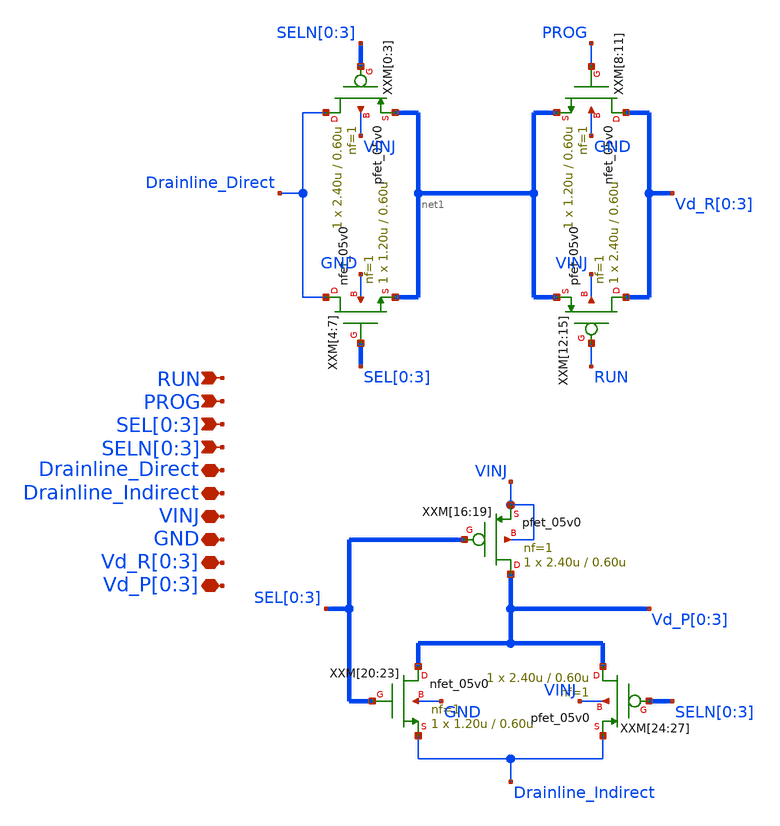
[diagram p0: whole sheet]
** sch_path: drain_switch/schematic/SWC_Drain.sch
**.subckt SWC_Drain RUN PROG SEL[0],SEL[1],SEL[2],SEL[3] SELN[0],SELN[1],SELN[2],SELN[3]
*+ Drainline_Direct Drainline_Indirect VINJ GND Vd_R[0],Vd_R[1],Vd_R[2],Vd_R[3] Vd_P[0],Vd_P[1],Vd_P[2],Vd_P[3]
*.ipin RUN
*.ipin PROG
*.ipin SEL[0],SEL[1],SEL[2],SEL[3]
*.ipin SELN[0],SELN[1],SELN[2],SELN[3]
*.iopin Drainline_Direct
*.iopin Drainline_Indirect
*.iopin VINJ
*.iopin GND
*.iopin Vd_R[0],Vd_R[1],Vd_R[2],Vd_R[3]
*.iopin Vd_P[0],Vd_P[1],Vd_P[2],Vd_P[3]
XXM[4] Drainline_Direct SEL[0] net1[3] GND nfet_05v0 L=0.60u W=1.20u nf=1 ad='int((nf+1)/2) * W/nf * 0.18u'
+ as='int((nf+2)/2) * W/nf * 0.18u' pd='2*int((nf+1)/2) * (W/nf + 0.18u)' ps='2*int((nf+2)/2) * (W/nf + 0.18u)'
+ nrd='0.18u / W' nrs='0.18u / W' sa=0 sb=0 sd=0 m=1
XXM[5] Drainline_Direct SEL[1] net1[2] GND nfet_05v0 L=0.60u W=1.20u nf=1 ad='int((nf+1)/2) * W/nf * 0.18u'
+ as='int((nf+2)/2) * W/nf * 0.18u' pd='2*int((nf+1)/2) * (W/nf + 0.18u)' ps='2*int((nf+2)/2) * (W/nf + 0.18u)'
+ nrd='0.18u / W' nrs='0.18u / W' sa=0 sb=0 sd=0 m=1
XXM[6] Drainline_Direct SEL[2] net1[1] GND nfet_05v0 L=0.60u W=1.20u nf=1 ad='int((nf+1)/2) * W/nf * 0.18u'
+ as='int((nf+2)/2) * W/nf * 0.18u' pd='2*int((nf+1)/2) * (W/nf + 0.18u)' ps='2*int((nf+2)/2) * (W/nf + 0.18u)'
+ nrd='0.18u / W' nrs='0.18u / W' sa=0 sb=0 sd=0 m=1
XXM[7] Drainline_Direct SEL[3] net1[0] GND nfet_05v0 L=0.60u W=1.20u nf=1 ad='int((nf+1)/2) * W/nf * 0.18u'
+ as='int((nf+2)/2) * W/nf * 0.18u' pd='2*int((nf+1)/2) * (W/nf + 0.18u)' ps='2*int((nf+2)/2) * (W/nf + 0.18u)'
+ nrd='0.18u / W' nrs='0.18u / W' sa=0 sb=0 sd=0 m=1
XXM[0] Drainline_Direct SELN[0] net1[3] VINJ pfet_05v0 L=0.60u W=2.40u nf=1 ad='int((nf+1)/2) * W/nf * 0.18u'
+ as='int((nf+2)/2) * W/nf * 0.18u' pd='2*int((nf+1)/2) * (W/nf + 0.18u)' ps='2*int((nf+2)/2) * (W/nf + 0.18u)'
+ nrd='0.18u / W' nrs='0.18u / W' sa=0 sb=0 sd=0 m=1
XXM[1] Drainline_Direct SELN[1] net1[2] VINJ pfet_05v0 L=0.60u W=2.40u nf=1 ad='int((nf+1)/2) * W/nf * 0.18u'
+ as='int((nf+2)/2) * W/nf * 0.18u' pd='2*int((nf+1)/2) * (W/nf + 0.18u)' ps='2*int((nf+2)/2) * (W/nf + 0.18u)'
+ nrd='0.18u / W' nrs='0.18u / W' sa=0 sb=0 sd=0 m=1
XXM[2] Drainline_Direct SELN[2] net1[1] VINJ pfet_05v0 L=0.60u W=2.40u nf=1 ad='int((nf+1)/2) * W/nf * 0.18u'
+ as='int((nf+2)/2) * W/nf * 0.18u' pd='2*int((nf+1)/2) * (W/nf + 0.18u)' ps='2*int((nf+2)/2) * (W/nf + 0.18u)'
+ nrd='0.18u / W' nrs='0.18u / W' sa=0 sb=0 sd=0 m=1
XXM[3] Drainline_Direct SELN[3] net1[0] VINJ pfet_05v0 L=0.60u W=2.40u nf=1 ad='int((nf+1)/2) * W/nf * 0.18u'
+ as='int((nf+2)/2) * W/nf * 0.18u' pd='2*int((nf+1)/2) * (W/nf + 0.18u)' ps='2*int((nf+2)/2) * (W/nf + 0.18u)'
+ nrd='0.18u / W' nrs='0.18u / W' sa=0 sb=0 sd=0 m=1
XXM[8] Vd_R[0] PROG net1[3] GND nfet_05v0 L=0.60u W=1.20u nf=1 ad='int((nf+1)/2) * W/nf * 0.18u' as='int((nf+2)/2) * W/nf * 0.18u'
+ pd='2*int((nf+1)/2) * (W/nf + 0.18u)' ps='2*int((nf+2)/2) * (W/nf + 0.18u)' nrd='0.18u / W' nrs='0.18u / W'
+ sa=0 sb=0 sd=0 m=1
XXM[9] Vd_R[1] PROG net1[2] GND nfet_05v0 L=0.60u W=1.20u nf=1 ad='int((nf+1)/2) * W/nf * 0.18u' as='int((nf+2)/2) * W/nf * 0.18u'
+ pd='2*int((nf+1)/2) * (W/nf + 0.18u)' ps='2*int((nf+2)/2) * (W/nf + 0.18u)' nrd='0.18u / W' nrs='0.18u / W'
+ sa=0 sb=0 sd=0 m=1
XXM[10] Vd_R[2] PROG net1[1] GND nfet_05v0 L=0.60u W=1.20u nf=1 ad='int((nf+1)/2) * W/nf * 0.18u' as='int((nf+2)/2) * W/nf * 0.18u'
+ pd='2*int((nf+1)/2) * (W/nf + 0.18u)' ps='2*int((nf+2)/2) * (W/nf + 0.18u)' nrd='0.18u / W' nrs='0.18u / W'
+ sa=0 sb=0 sd=0 m=1
XXM[11] Vd_R[3] PROG net1[0] GND nfet_05v0 L=0.60u W=1.20u nf=1 ad='int((nf+1)/2) * W/nf * 0.18u' as='int((nf+2)/2) * W/nf * 0.18u'
+ pd='2*int((nf+1)/2) * (W/nf + 0.18u)' ps='2*int((nf+2)/2) * (W/nf + 0.18u)' nrd='0.18u / W' nrs='0.18u / W'
+ sa=0 sb=0 sd=0 m=1
XXM[12] Vd_R[0] RUN net1[3] VINJ pfet_05v0 L=0.60u W=2.40u nf=1 ad='int((nf+1)/2) * W/nf * 0.18u' as='int((nf+2)/2) * W/nf * 0.18u'
+ pd='2*int((nf+1)/2) * (W/nf + 0.18u)' ps='2*int((nf+2)/2) * (W/nf + 0.18u)' nrd='0.18u / W' nrs='0.18u / W'
+ sa=0 sb=0 sd=0 m=1
XXM[13] Vd_R[1] RUN net1[2] VINJ pfet_05v0 L=0.60u W=2.40u nf=1 ad='int((nf+1)/2) * W/nf * 0.18u' as='int((nf+2)/2) * W/nf * 0.18u'
+ pd='2*int((nf+1)/2) * (W/nf + 0.18u)' ps='2*int((nf+2)/2) * (W/nf + 0.18u)' nrd='0.18u / W' nrs='0.18u / W'
+ sa=0 sb=0 sd=0 m=1
XXM[14] Vd_R[2] RUN net1[1] VINJ pfet_05v0 L=0.60u W=2.40u nf=1 ad='int((nf+1)/2) * W/nf * 0.18u' as='int((nf+2)/2) * W/nf * 0.18u'
+ pd='2*int((nf+1)/2) * (W/nf + 0.18u)' ps='2*int((nf+2)/2) * (W/nf + 0.18u)' nrd='0.18u / W' nrs='0.18u / W'
+ sa=0 sb=0 sd=0 m=1
XXM[15] Vd_R[3] RUN net1[0] VINJ pfet_05v0 L=0.60u W=2.40u nf=1 ad='int((nf+1)/2) * W/nf * 0.18u' as='int((nf+2)/2) * W/nf * 0.18u'
+ pd='2*int((nf+1)/2) * (W/nf + 0.18u)' ps='2*int((nf+2)/2) * (W/nf + 0.18u)' nrd='0.18u / W' nrs='0.18u / W'
+ sa=0 sb=0 sd=0 m=1
XXM[20] Vd_P[0] SEL[0] Drainline_Indirect GND nfet_05v0 L=0.60u W=1.20u nf=1 ad='int((nf+1)/2) * W/nf * 0.18u'
+ as='int((nf+2)/2) * W/nf * 0.18u' pd='2*int((nf+1)/2) * (W/nf + 0.18u)' ps='2*int((nf+2)/2) * (W/nf + 0.18u)'
+ nrd='0.18u / W' nrs='0.18u / W' sa=0 sb=0 sd=0 m=1
XXM[21] Vd_P[1] SEL[1] Drainline_Indirect GND nfet_05v0 L=0.60u W=1.20u nf=1 ad='int((nf+1)/2) * W/nf * 0.18u'
+ as='int((nf+2)/2) * W/nf * 0.18u' pd='2*int((nf+1)/2) * (W/nf + 0.18u)' ps='2*int((nf+2)/2) * (W/nf + 0.18u)'
+ nrd='0.18u / W' nrs='0.18u / W' sa=0 sb=0 sd=0 m=1
XXM[22] Vd_P[2] SEL[2] Drainline_Indirect GND nfet_05v0 L=0.60u W=1.20u nf=1 ad='int((nf+1)/2) * W/nf * 0.18u'
+ as='int((nf+2)/2) * W/nf * 0.18u' pd='2*int((nf+1)/2) * (W/nf + 0.18u)' ps='2*int((nf+2)/2) * (W/nf + 0.18u)'
+ nrd='0.18u / W' nrs='0.18u / W' sa=0 sb=0 sd=0 m=1
XXM[23] Vd_P[3] SEL[3] Drainline_Indirect GND nfet_05v0 L=0.60u W=1.20u nf=1 ad='int((nf+1)/2) * W/nf * 0.18u'
+ as='int((nf+2)/2) * W/nf * 0.18u' pd='2*int((nf+1)/2) * (W/nf + 0.18u)' ps='2*int((nf+2)/2) * (W/nf + 0.18u)'
+ nrd='0.18u / W' nrs='0.18u / W' sa=0 sb=0 sd=0 m=1
XXM[24] Vd_P[0] SELN[0] Drainline_Indirect VINJ pfet_05v0 L=0.60u W=2.40u nf=1 ad='int((nf+1)/2) * W/nf * 0.18u'
+ as='int((nf+2)/2) * W/nf * 0.18u' pd='2*int((nf+1)/2) * (W/nf + 0.18u)' ps='2*int((nf+2)/2) * (W/nf + 0.18u)'
+ nrd='0.18u / W' nrs='0.18u / W' sa=0 sb=0 sd=0 m=1
XXM[25] Vd_P[1] SELN[1] Drainline_Indirect VINJ pfet_05v0 L=0.60u W=2.40u nf=1 ad='int((nf+1)/2) * W/nf * 0.18u'
+ as='int((nf+2)/2) * W/nf * 0.18u' pd='2*int((nf+1)/2) * (W/nf + 0.18u)' ps='2*int((nf+2)/2) * (W/nf + 0.18u)'
+ nrd='0.18u / W' nrs='0.18u / W' sa=0 sb=0 sd=0 m=1
XXM[26] Vd_P[2] SELN[2] Drainline_Indirect VINJ pfet_05v0 L=0.60u W=2.40u nf=1 ad='int((nf+1)/2) * W/nf * 0.18u'
+ as='int((nf+2)/2) * W/nf * 0.18u' pd='2*int((nf+1)/2) * (W/nf + 0.18u)' ps='2*int((nf+2)/2) * (W/nf + 0.18u)'
+ nrd='0.18u / W' nrs='0.18u / W' sa=0 sb=0 sd=0 m=1
XXM[27] Vd_P[3] SELN[3] Drainline_Indirect VINJ pfet_05v0 L=0.60u W=2.40u nf=1 ad='int((nf+1)/2) * W/nf * 0.18u'
+ as='int((nf+2)/2) * W/nf * 0.18u' pd='2*int((nf+1)/2) * (W/nf + 0.18u)' ps='2*int((nf+2)/2) * (W/nf + 0.18u)'
+ nrd='0.18u / W' nrs='0.18u / W' sa=0 sb=0 sd=0 m=1
XXM[16] Vd_P[0] SEL[0] VINJ VINJ pfet_05v0 L=0.60u W=2.40u nf=1 ad='int((nf+1)/2) * W/nf * 0.18u' as='int((nf+2)/2) * W/nf * 0.18u'
+ pd='2*int((nf+1)/2) * (W/nf + 0.18u)' ps='2*int((nf+2)/2) * (W/nf + 0.18u)' nrd='0.18u / W' nrs='0.18u / W'
+ sa=0 sb=0 sd=0 m=1
XXM[17] Vd_P[1] SEL[1] VINJ VINJ pfet_05v0 L=0.60u W=2.40u nf=1 ad='int((nf+1)/2) * W/nf * 0.18u' as='int((nf+2)/2) * W/nf * 0.18u'
+ pd='2*int((nf+1)/2) * (W/nf + 0.18u)' ps='2*int((nf+2)/2) * (W/nf + 0.18u)' nrd='0.18u / W' nrs='0.18u / W'
+ sa=0 sb=0 sd=0 m=1
XXM[18] Vd_P[2] SEL[2] VINJ VINJ pfet_05v0 L=0.60u W=2.40u nf=1 ad='int((nf+1)/2) * W/nf * 0.18u' as='int((nf+2)/2) * W/nf * 0.18u'
+ pd='2*int((nf+1)/2) * (W/nf + 0.18u)' ps='2*int((nf+2)/2) * (W/nf + 0.18u)' nrd='0.18u / W' nrs='0.18u / W'
+ sa=0 sb=0 sd=0 m=1
XXM[19] Vd_P[3] SEL[3] VINJ VINJ pfet_05v0 L=0.60u W=2.40u nf=1 ad='int((nf+1)/2) * W/nf * 0.18u' as='int((nf+2)/2) * W/nf * 0.18u'
+ pd='2*int((nf+1)/2) * (W/nf + 0.18u)' ps='2*int((nf+2)/2) * (W/nf + 0.18u)' nrd='0.18u / W' nrs='0.18u / W'
+ sa=0 sb=0 sd=0 m=1
**.ends
.end
